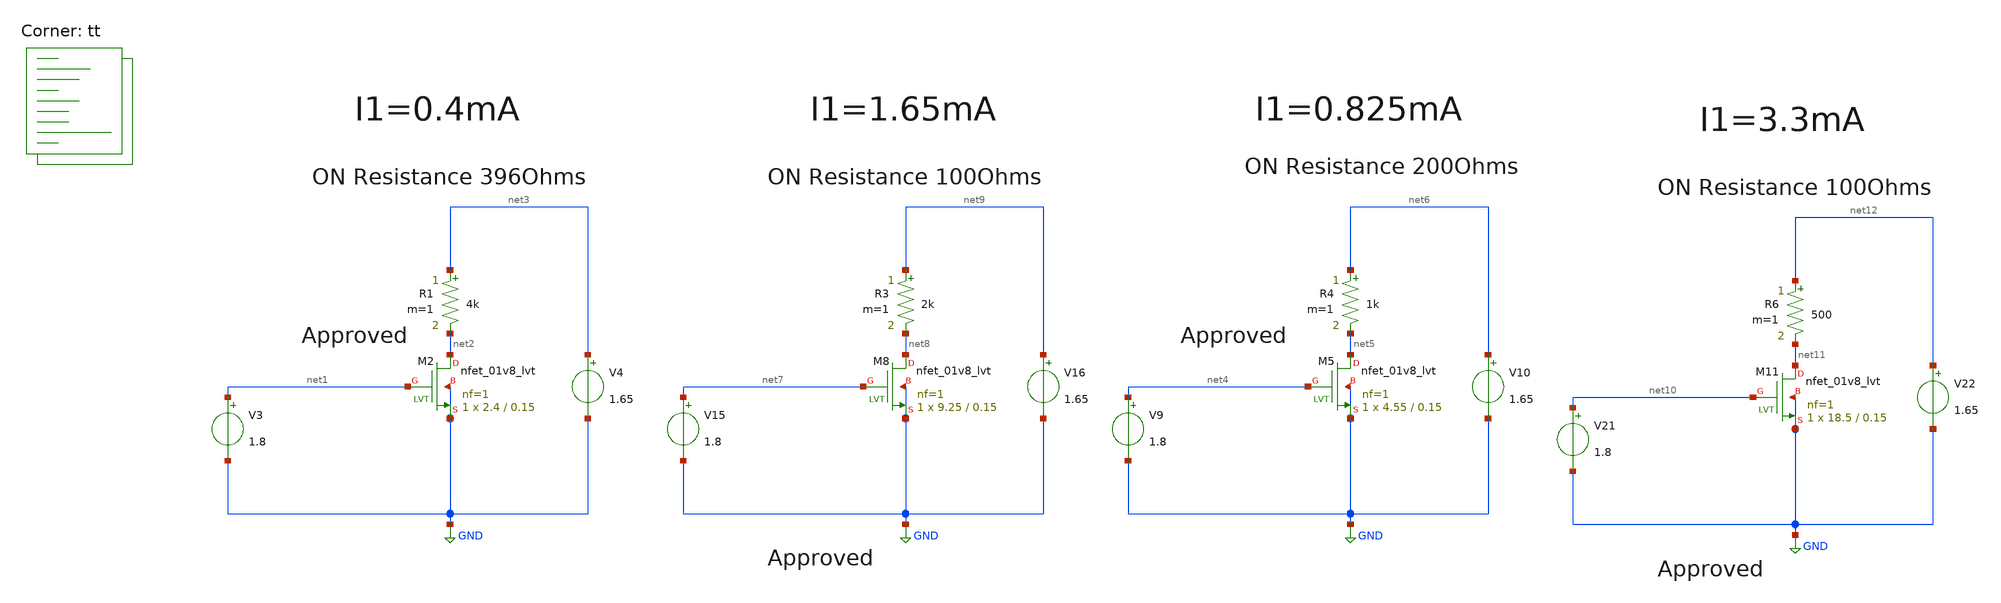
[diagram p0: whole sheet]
** sch_path: Switch-Res/Schematics/Res2try.sch
**.subckt Res2try
V3 net1 GND 1.8
V4 net3 GND 1.65
XM2 net2 net1 GND GND sky130_fd_pr__nfet_01v8_lvt L=0.15 W=2.4 nf=1 ad='int((nf+1)/2) * W/nf * 0.29'
+ as='int((nf+2)/2) * W/nf * 0.29' pd='2*int((nf+1)/2) * (W/nf + 0.29)' ps='2*int((nf+2)/2) * (W/nf + 0.29)'
+ nrd='0.29 / W' nrs='0.29 / W' sa=0 sb=0 sd=0 mult=1 m=1
V9 net4 GND 1.8
V10 net6 GND 1.65
XM5 net5 net4 GND GND sky130_fd_pr__nfet_01v8_lvt L=0.15 W=4.55 nf=1 ad='int((nf+1)/2) * W/nf * 0.29'
+ as='int((nf+2)/2) * W/nf * 0.29' pd='2*int((nf+1)/2) * (W/nf + 0.29)' ps='2*int((nf+2)/2) * (W/nf + 0.29)'
+ nrd='0.29 / W' nrs='0.29 / W' sa=0 sb=0 sd=0 mult=1 m=1
V15 net7 GND 1.8
V16 net9 GND 1.65
XM8 net8 net7 GND GND sky130_fd_pr__nfet_01v8_lvt L=0.15 W=9.25 nf=1 ad='int((nf+1)/2) * W/nf * 0.29'
+ as='int((nf+2)/2) * W/nf * 0.29' pd='2*int((nf+1)/2) * (W/nf + 0.29)' ps='2*int((nf+2)/2) * (W/nf + 0.29)'
+ nrd='0.29 / W' nrs='0.29 / W' sa=0 sb=0 sd=0 mult=1 m=1
V21 net10 GND 1.8
V22 net12 GND 1.65
XM11 net11 net10 GND GND sky130_fd_pr__nfet_01v8_lvt L=0.15 W=18.5 nf=1 ad='int((nf+1)/2) * W/nf * 0.29'
+ as='int((nf+2)/2) * W/nf * 0.29' pd='2*int((nf+1)/2) * (W/nf + 0.29)' ps='2*int((nf+2)/2) * (W/nf + 0.29)'
+ nrd='0.29 / W' nrs='0.29 / W' sa=0 sb=0 sd=0 mult=1 m=1
R1 net3 net2 4k m=1
R3 net9 net8 2k m=1
R4 net6 net5 1k m=1
R6 net12 net11 500 m=1
**** begin user architecture code


.option wnflag=1
.option savecurrents
.temp 27
.control
save all
write Res2try.raw
set appendwrite
op
show m : gm : gmbs : gds : vds : vdsat : vgs : vth : id: cgg
write Res2try.raw
tran 1m 10m 1m
.endc

.lib $::SKYWATER_MODELS/sky130.lib.spice tt
**** end user architecture code
**.ends
.GLOBAL GND
.end
